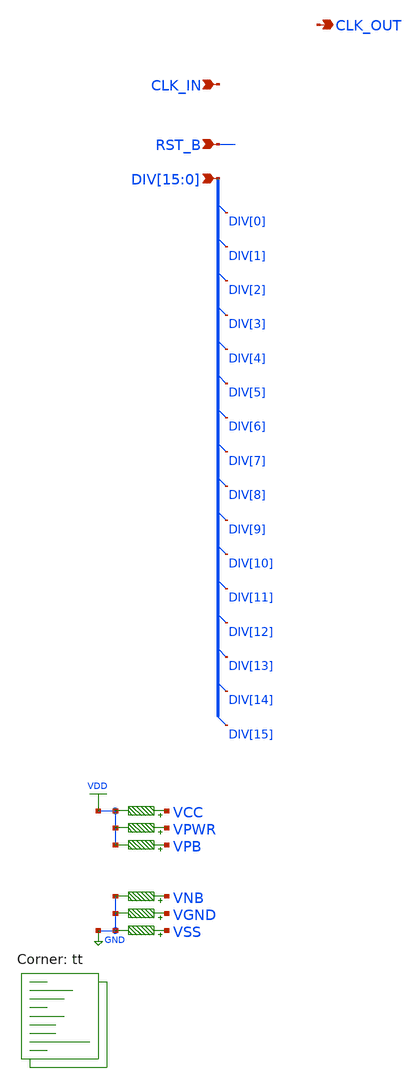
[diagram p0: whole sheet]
** sch_path: dig_dly.sch
**.subckt dig_dly CLK_OUT CLK_IN RST_B
*+ DIV[15],DIV[14],DIV[13],DIV[12],DIV[11],DIV[10],DIV[9],DIV[8],DIV[7],DIV[6],DIV[5],DIV[4],DIV[3],DIV[2],DIV[1],DIV[0]
*.opin CLK_OUT
*.ipin CLK_IN
*.ipin RST_B
*.ipin
*+ DIV[15],DIV[14],DIV[13],DIV[12],DIV[11],DIV[10],DIV[9],DIV[8],DIV[7],DIV[6],DIV[5],DIV[4],DIV[3],DIV[2],DIV[1],DIV[0]
R1 VNB GND 0.01 m=1
R2 VPB VDD 0.01 m=1
R3 VPWR VDD 0.01 m=1
R4 VGND GND 0.01 m=1
R5 VSS GND 0.01 m=1
R6 VCC VDD 0.01 m=1
**** begin user architecture code
.lib $::SKYWATER_MODELS/sky130.lib.spice tt


.include /usr/local/share/pdk/sky130A/libs.ref/sky130_fd_sc_hd/spice/sky130_fd_sc_hd.spice tt
.control
  save all
  tran .1n 10u
  write top.raw
  quit 0
.endc


**** end user architecture code
**.ends
.GLOBAL GND
.GLOBAL VDD
.end
